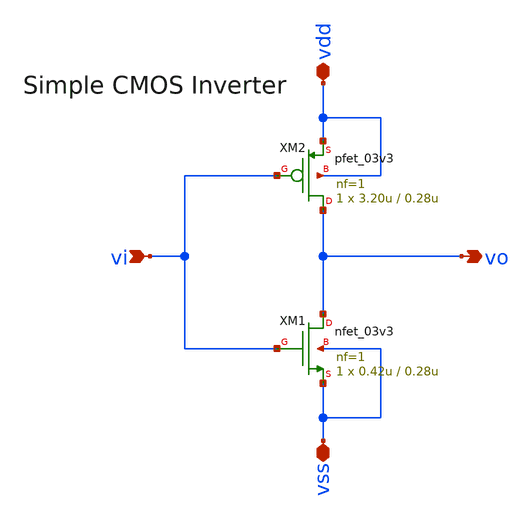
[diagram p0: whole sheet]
** sch_path: xschem/sar_adc/blocks/comparator/comp_inv_3v3.sch
**.subckt comp_inv_3v3 vi vo vdd vss
*.ipin vi
*.opin vo
*.iopin vdd
*.iopin vss
XM2 vo vi vdd vdd pfet_03v3 L=0.28u W=3.20u nf=1 ad='int((nf+1)/2) * W/nf * 0.18u' as='int((nf+2)/2) * W/nf * 0.18u'
+ pd='2*int((nf+1)/2) * (W/nf + 0.18u)' ps='2*int((nf+2)/2) * (W/nf + 0.18u)' nrd='0.18u / W' nrs='0.18u / W'
+ sa=0 sb=0 sd=0 m=1
XM1 vo vi vss vss nfet_03v3 L=0.28u W=0.42u nf=1 ad='int((nf+1)/2) * W/nf * 0.18u' as='int((nf+2)/2) * W/nf * 0.18u'
+ pd='2*int((nf+1)/2) * (W/nf + 0.18u)' ps='2*int((nf+2)/2) * (W/nf + 0.18u)' nrd='0.18u / W' nrs='0.18u / W'
+ sa=0 sb=0 sd=0 m=1
**.ends
.end
